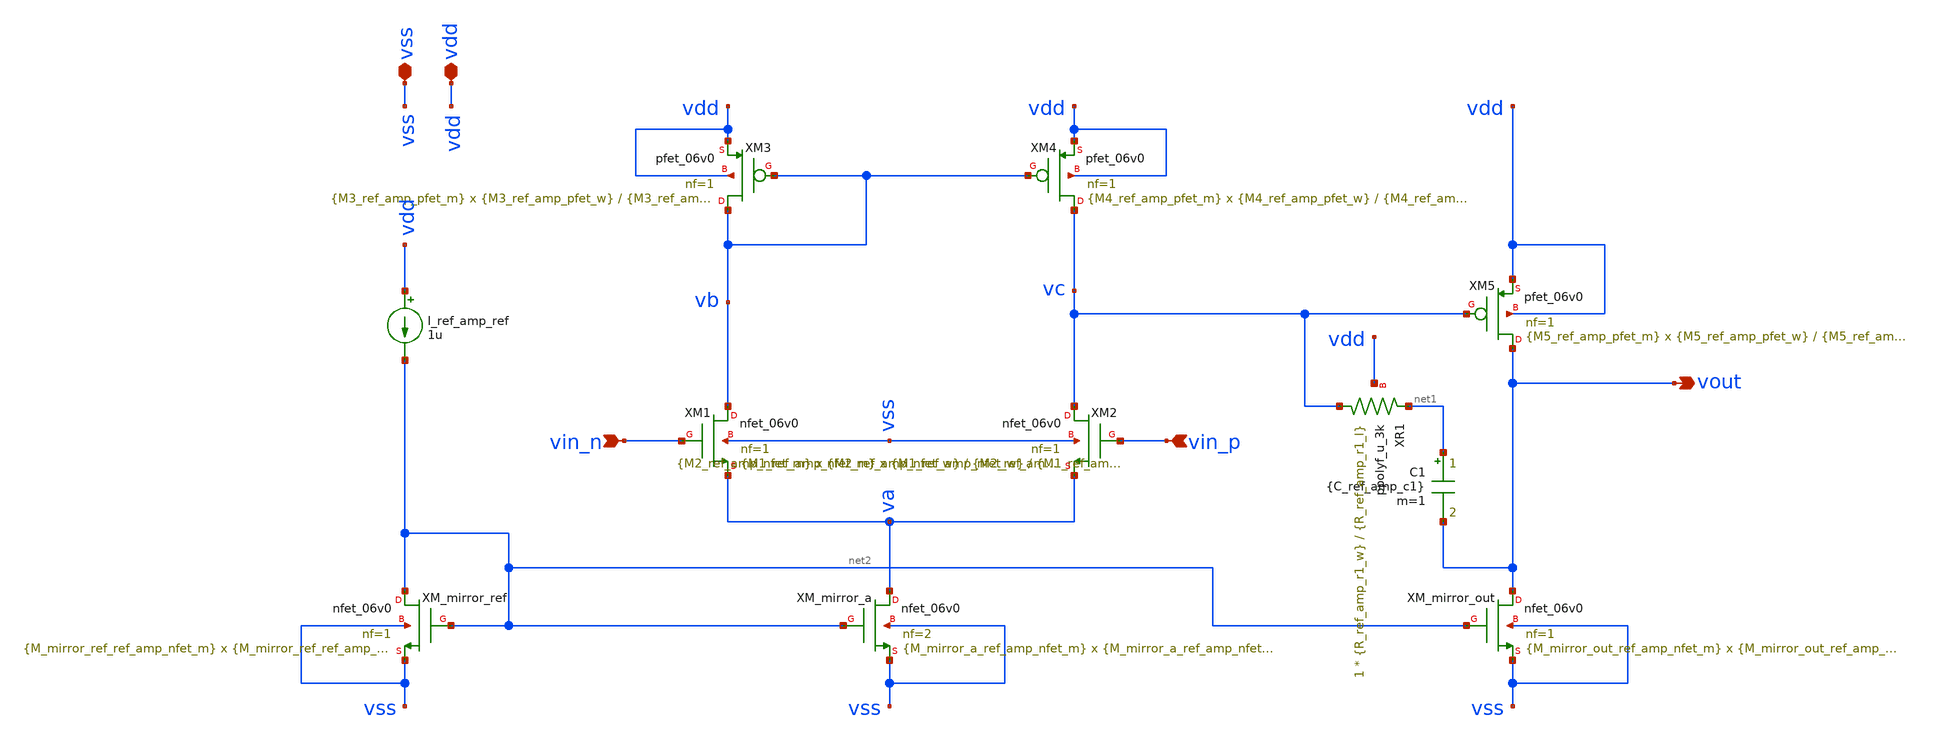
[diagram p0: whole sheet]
** sch_path: analog-db/circuits/ldo_005_buffered_ref/reference/ti-ldo/ref_amp/ref_amp.sch
**.subckt ref_amp vin_n vin_p vdd vss vout
*.ipin vin_n
*.ipin vin_p
*.iopin vdd
*.iopin vss
*.opin vout
XM1 vb vin_n va vss nfet_06v0 L={M1_ref_amp_nfet_l} W={M1_ref_amp_nfet_w} nf=1 ad='int((nf+1)/2) * W/nf * 0.18u'
+ as='int((nf+2)/2) * W/nf * 0.18u' pd='2*int((nf+1)/2) * (W/nf + 0.18u)' ps='2*int((nf+2)/2) * (W/nf + 0.18u)'
+ nrd='0.18u / W' nrs='0.18u / W' sa=0 sb=0 sd=0 m={M1_ref_amp_nfet_m}
XM2 vc vin_p va vss nfet_06v0 L={M2_ref_amp_nfet_l} W={M2_ref_amp_nfet_w} nf=1 ad='int((nf+1)/2) * W/nf * 0.18u'
+ as='int((nf+2)/2) * W/nf * 0.18u' pd='2*int((nf+1)/2) * (W/nf + 0.18u)' ps='2*int((nf+2)/2) * (W/nf + 0.18u)'
+ nrd='0.18u / W' nrs='0.18u / W' sa=0 sb=0 sd=0 m={M2_ref_amp_nfet_m}
XM3 vb vb vdd vdd pfet_06v0 L={M3_ref_amp_pfet_l} W={M3_ref_amp_pfet_w} nf=1 ad='int((nf+1)/2) * W/nf * 0.18u'
+ as='int((nf+2)/2) * W/nf * 0.18u' pd='2*int((nf+1)/2) * (W/nf + 0.18u)' ps='2*int((nf+2)/2) * (W/nf + 0.18u)'
+ nrd='0.18u / W' nrs='0.18u / W' sa=0 sb=0 sd=0 m={M3_ref_amp_pfet_m}
XM4 vc vb vdd vdd pfet_06v0 L={M4_ref_amp_pfet_l} W={M4_ref_amp_pfet_w} nf=1 ad='int((nf+1)/2) * W/nf * 0.18u'
+ as='int((nf+2)/2) * W/nf * 0.18u' pd='2*int((nf+1)/2) * (W/nf + 0.18u)' ps='2*int((nf+2)/2) * (W/nf + 0.18u)'
+ nrd='0.18u / W' nrs='0.18u / W' sa=0 sb=0 sd=0 m={M4_ref_amp_pfet_m}
XM5 vout vc vdd vdd pfet_06v0 L={M5_ref_amp_pfet_l} W={M5_ref_amp_pfet_w} nf=1 ad='int((nf+1)/2) * W/nf * 0.18u'
+ as='int((nf+2)/2) * W/nf * 0.18u' pd='2*int((nf+1)/2) * (W/nf + 0.18u)' ps='2*int((nf+2)/2) * (W/nf + 0.18u)'
+ nrd='0.18u / W' nrs='0.18u / W' sa=0 sb=0 sd=0 m={M5_ref_amp_pfet_m}
C1 net1 vout {C_ref_amp_c1} m=1
XR1 vc net1 vdd ppolyf_u_3k r_width={R_ref_amp_r1_w} r_length={R_ref_amp_r1_l} m=1
I_ref_amp_ref vdd net2 1u
XM_mirror_a va net2 vss vss nfet_06v0 L={M_mirror_a_ref_amp_nfet_l} W={M_mirror_a_ref_amp_nfet_w} nf=2
+ ad='int((nf+1)/2) * W/nf * 0.18u' as='int((nf+2)/2) * W/nf * 0.18u' pd='2*int((nf+1)/2) * (W/nf + 0.18u)'
+ ps='2*int((nf+2)/2) * (W/nf + 0.18u)' nrd='0.18u / W' nrs='0.18u / W' sa=0 sb=0 sd=0 m={M_mirror_a_ref_amp_nfet_m}
XM_mirror_out vout net2 vss vss nfet_06v0 L={M_mirror_out_ref_amp_nfet_l} W={M_mirror_out_ref_amp_nfet_w}
+ nf=1 ad='int((nf+1)/2) * W/nf * 0.18u' as='int((nf+2)/2) * W/nf * 0.18u' pd='2*int((nf+1)/2) * (W/nf + 0.18u)'
+ ps='2*int((nf+2)/2) * (W/nf + 0.18u)' nrd='0.18u / W' nrs='0.18u / W' sa=0 sb=0 sd=0 m={M_mirror_out_ref_amp_nfet_m}
XM_mirror_ref net2 net2 vss vss nfet_06v0 L={M_mirror_ref_ref_amp_nfet_l} W={M_mirror_ref_ref_amp_nfet_w}
+ nf=1 ad='int((nf+1)/2) * W/nf * 0.18u' as='int((nf+2)/2) * W/nf * 0.18u' pd='2*int((nf+1)/2) * (W/nf + 0.18u)'
+ ps='2*int((nf+2)/2) * (W/nf + 0.18u)' nrd='0.18u / W' nrs='0.18u / W' sa=0 sb=0 sd=0 m={M_mirror_ref_ref_amp_nfet_m}
**.ends
.end
